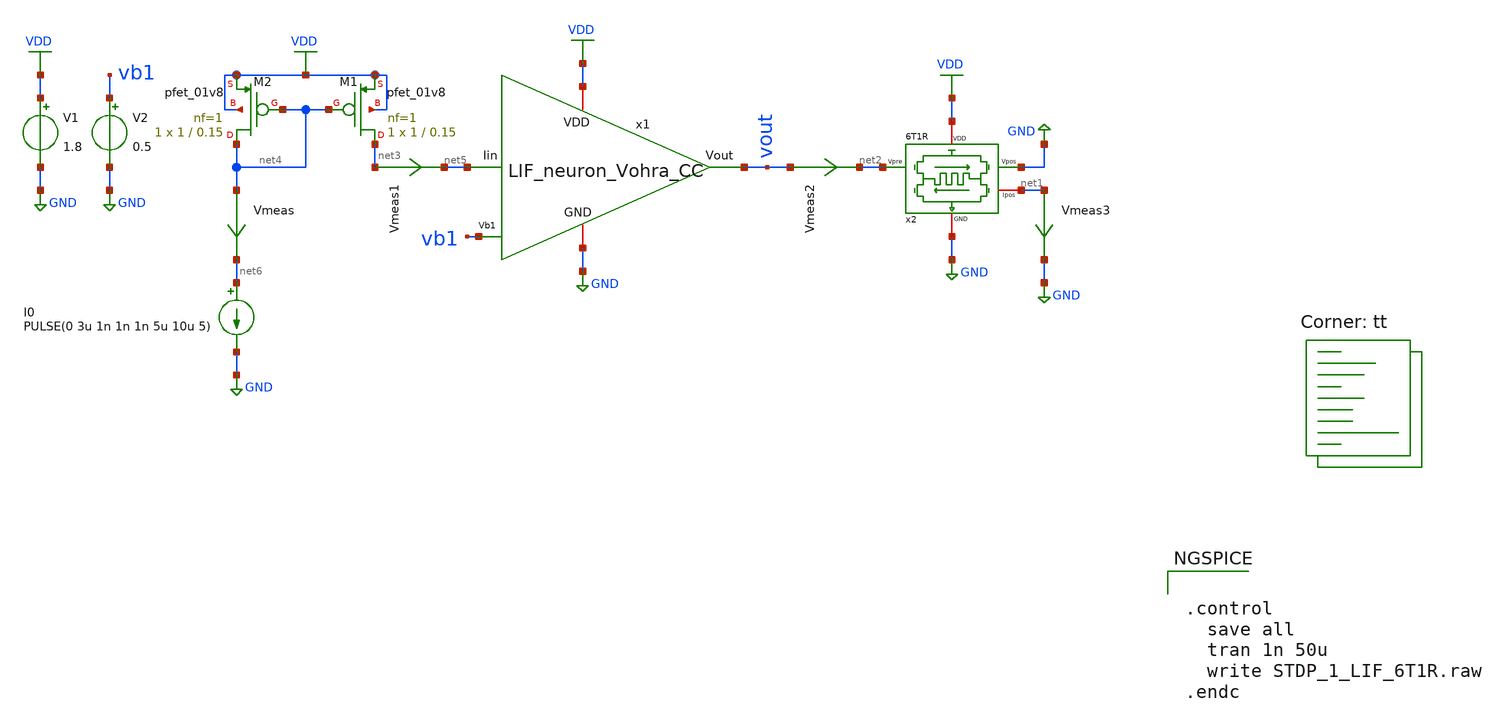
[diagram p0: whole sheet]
** sch_path: STDP/STDP_1_LIF_6T1R.sch
**.subckt STDP_1_LIF_6T1R
V1 VDD GND 1.8
V2 vb1 GND 0.5
x2 VDD net1 net2 GND GND 6T1R
x1 VDD vout vb1 GND net5 LIF_neuron_Vohra_CC
I0 net6 GND PULSE(0 3u 1n 1n 1n 5u 10u 5)
XM1 net3 net4 VDD VDD sky130_fd_pr__pfet_01v8 L=0.15 W=1 nf=1 ad='int((nf+1)/2) * W/nf * 0.29' as='int((nf+2)/2) * W/nf * 0.29'
+ pd='2*int((nf+1)/2) * (W/nf + 0.29)' ps='2*int((nf+2)/2) * (W/nf + 0.29)' nrd='0.29 / W' nrs='0.29 / W'
+ sa=0 sb=0 sd=0 mult=1 m=1
XM2 net4 net4 VDD VDD sky130_fd_pr__pfet_01v8 L=0.15 W=1 nf=1 ad='int((nf+1)/2) * W/nf * 0.29' as='int((nf+2)/2) * W/nf * 0.29'
+ pd='2*int((nf+1)/2) * (W/nf + 0.29)' ps='2*int((nf+2)/2) * (W/nf + 0.29)' nrd='0.29 / W' nrs='0.29 / W'
+ sa=0 sb=0 sd=0 mult=1 m=1
Vmeas net4 net6 0
.save i(vmeas)
Vmeas1 net3 net5 0
.save i(vmeas1)
Vmeas2 vout net2 0
.save i(vmeas2)
Vmeas3 net1 GND 0
.save i(vmeas3)
**** begin user architecture code
.lib $::SKYWATER_MODELS/sky130.lib.spice tt

** opencircuitdesign pdks install
.inc $::SKYWATER_MODELS/rram_v0.spice



.control
  save all
  tran 1n 50u
  write STDP_1_LIF_6T1R.raw
.endc


**** end user architecture code
**.ends

* expanding   symbol:  /home/ricardoatt/RATT_repos/Proyectos_xschem/synapse/6T1R.sym # of pins=5
** sym_path: synapse/6T1R.sym
** sch_path: synapse/6T1R.sch
.subckt 6T1R VDD Ipos Vpre Vpos GND
*.ipin Vpre
*.ipin Vpos
*.iopin GND
*.iopin Ipos
*.iopin VDD
XM1 BE Vpre vipre GND sky130_fd_pr__nfet_01v8 L=0.15 W=10 nf=1 ad='int((nf+1)/2) * W/nf * 0.29' as='int((nf+2)/2) * W/nf * 0.29'
+ pd='2*int((nf+1)/2) * (W/nf + 0.29)' ps='2*int((nf+2)/2) * (W/nf + 0.29)' nrd='0.29 / W' nrs='0.29 / W'
+ sa=0 sb=0 sd=0 mult=1 m=1
XR1 TE BE rram_v0
XM3 TE Vpos vipre GND sky130_fd_pr__nfet_01v8 L=0.15 W=15 nf=1 ad='int((nf+1)/2) * W/nf * 0.29' as='int((nf+2)/2) * W/nf * 0.29'
+ pd='2*int((nf+1)/2) * (W/nf + 0.29)' ps='2*int((nf+2)/2) * (W/nf + 0.29)' nrd='0.29 / W' nrs='0.29 / W'
+ sa=0 sb=0 sd=0 mult=1 m=1
XM6 Ipos vipre VDD VDD sky130_fd_pr__pfet_01v8 L=0.15 W=20 nf=1 ad='int((nf+1)/2) * W/nf * 0.29' as='int((nf+2)/2) * W/nf * 0.29'
+ pd='2*int((nf+1)/2) * (W/nf + 0.29)' ps='2*int((nf+2)/2) * (W/nf + 0.29)' nrd='0.29 / W' nrs='0.29 / W'
+ sa=0 sb=0 sd=0 mult=1 m=1
XM5 vipre vipre VDD VDD sky130_fd_pr__pfet_01v8 L=0.15 W=20 nf=1 ad='int((nf+1)/2) * W/nf * 0.29' as='int((nf+2)/2) * W/nf * 0.29'
+ pd='2*int((nf+1)/2) * (W/nf + 0.29)' ps='2*int((nf+2)/2) * (W/nf + 0.29)' nrd='0.29 / W' nrs='0.29 / W'
+ sa=0 sb=0 sd=0 mult=1 m=1
XM2 GND Vpos BE GND sky130_fd_pr__nfet_01v8 L=0.15 W=15 nf=1 ad='int((nf+1)/2) * W/nf * 0.29' as='int((nf+2)/2) * W/nf * 0.29'
+ pd='2*int((nf+1)/2) * (W/nf + 0.29)' ps='2*int((nf+2)/2) * (W/nf + 0.29)' nrd='0.29 / W' nrs='0.29 / W'
+ sa=0 sb=0 sd=0 mult=1 m=1
XM4 GND Vpre TE GND sky130_fd_pr__nfet_01v8 L=0.15 W=10 nf=1 ad='int((nf+1)/2) * W/nf * 0.29' as='int((nf+2)/2) * W/nf * 0.29'
+ pd='2*int((nf+1)/2) * (W/nf + 0.29)' ps='2*int((nf+2)/2) * (W/nf + 0.29)' nrd='0.29 / W' nrs='0.29 / W'
+ sa=0 sb=0 sd=0 mult=1 m=1
.ends


* expanding   symbol:
*+  /home/ricardoatt/RATT_repos/Proyectos_xschem/LIF_neuron/LIF_neuron_Vohra_CC.sym # of pins=5
** sym_path: LIF_neuron/LIF_neuron_Vohra_CC.sym
** sch_path: LIF_neuron/LIF_neuron_Vohra_CC.sch
.subckt LIF_neuron_Vohra_CC VDD Vout Vb1 GND Iin
*.iopin GND
*.ipin Vb1
*.iopin VDD
*.opin Vout
*.ipin Iin
XM13 net2 Vb1 GND GND sky130_fd_pr__nfet_01v8 L=0.5 W=5 nf=1 ad='int((nf+1)/2) * W/nf * 0.29' as='int((nf+2)/2) * W/nf * 0.29'
+ pd='2*int((nf+1)/2) * (W/nf + 0.29)' ps='2*int((nf+2)/2) * (W/nf + 0.29)' nrd='0.29 / W' nrs='0.29 / W'
+ sa=0 sb=0 sd=0 mult=1 m=1
XM12 rc net1 net2 GND sky130_fd_pr__nfet_01v8 L=1 W=1 nf=1 ad='int((nf+1)/2) * W/nf * 0.29' as='int((nf+2)/2) * W/nf * 0.29'
+ pd='2*int((nf+1)/2) * (W/nf + 0.29)' ps='2*int((nf+2)/2) * (W/nf + 0.29)' nrd='0.29 / W' nrs='0.29 / W'
+ sa=0 sb=0 sd=0 mult=1 m=1
XM11 rc net1 VDD VDD sky130_fd_pr__pfet_01v8 L=1 W=1 nf=1 ad='int((nf+1)/2) * W/nf * 0.29' as='int((nf+2)/2) * W/nf * 0.29'
+ pd='2*int((nf+1)/2) * (W/nf + 0.29)' ps='2*int((nf+2)/2) * (W/nf + 0.29)' nrd='0.29 / W' nrs='0.29 / W'
+ sa=0 sb=0 sd=0 mult=1 m=1
XC1 rc GND sky130_fd_pr__cap_mim_m3_1 W=21 L=1 MF=1 m=1
XM14 Iin rc GND GND sky130_fd_pr__nfet_01v8 L=15 W=1 nf=1 ad='int((nf+1)/2) * W/nf * 0.29' as='int((nf+2)/2) * W/nf * 0.29'
+ pd='2*int((nf+1)/2) * (W/nf + 0.29)' ps='2*int((nf+2)/2) * (W/nf + 0.29)' nrd='0.29 / W' nrs='0.29 / W'
+ sa=0 sb=0 sd=0 mult=1 m=1
XC2 Iin GND sky130_fd_pr__cap_mim_m3_1 W=10 L=1 MF=50 m=50
XM6 net3 Vout GND GND sky130_fd_pr__nfet_01v8 L=0.5 W=1 nf=1 ad='int((nf+1)/2) * W/nf * 0.29' as='int((nf+2)/2) * W/nf * 0.29'
+ pd='2*int((nf+1)/2) * (W/nf + 0.29)' ps='2*int((nf+2)/2) * (W/nf + 0.29)' nrd='0.29 / W' nrs='0.29 / W'
+ sa=0 sb=0 sd=0 mult=1 m=1
XM7 net1 Iin net3 GND sky130_fd_pr__nfet_01v8 L=1 W=1 nf=1 ad='int((nf+1)/2) * W/nf * 0.29' as='int((nf+2)/2) * W/nf * 0.29'
+ pd='2*int((nf+1)/2) * (W/nf + 0.29)' ps='2*int((nf+2)/2) * (W/nf + 0.29)' nrd='0.29 / W' nrs='0.29 / W'
+ sa=0 sb=0 sd=0 mult=1 m=1
XM8 net1 Iin VDD VDD sky130_fd_pr__pfet_01v8 L=1 W=1 nf=1 ad='int((nf+1)/2) * W/nf * 0.29' as='int((nf+2)/2) * W/nf * 0.29'
+ pd='2*int((nf+1)/2) * (W/nf + 0.29)' ps='2*int((nf+2)/2) * (W/nf + 0.29)' nrd='0.29 / W' nrs='0.29 / W'
+ sa=0 sb=0 sd=0 mult=1 m=1
XM9 Vout net1 net3 GND sky130_fd_pr__nfet_01v8 L=1 W=1 nf=1 ad='int((nf+1)/2) * W/nf * 0.29' as='int((nf+2)/2) * W/nf * 0.29'
+ pd='2*int((nf+1)/2) * (W/nf + 0.29)' ps='2*int((nf+2)/2) * (W/nf + 0.29)' nrd='0.29 / W' nrs='0.29 / W'
+ sa=0 sb=0 sd=0 mult=1 m=1
XM10 Vout net1 VDD VDD sky130_fd_pr__pfet_01v8 L=1 W=5 nf=1 ad='int((nf+1)/2) * W/nf * 0.29' as='int((nf+2)/2) * W/nf * 0.29'
+ pd='2*int((nf+1)/2) * (W/nf + 0.29)' ps='2*int((nf+2)/2) * (W/nf + 0.29)' nrd='0.29 / W' nrs='0.29 / W'
+ sa=0 sb=0 sd=0 mult=1 m=1
.ends

.GLOBAL GND
.GLOBAL VDD
.end
